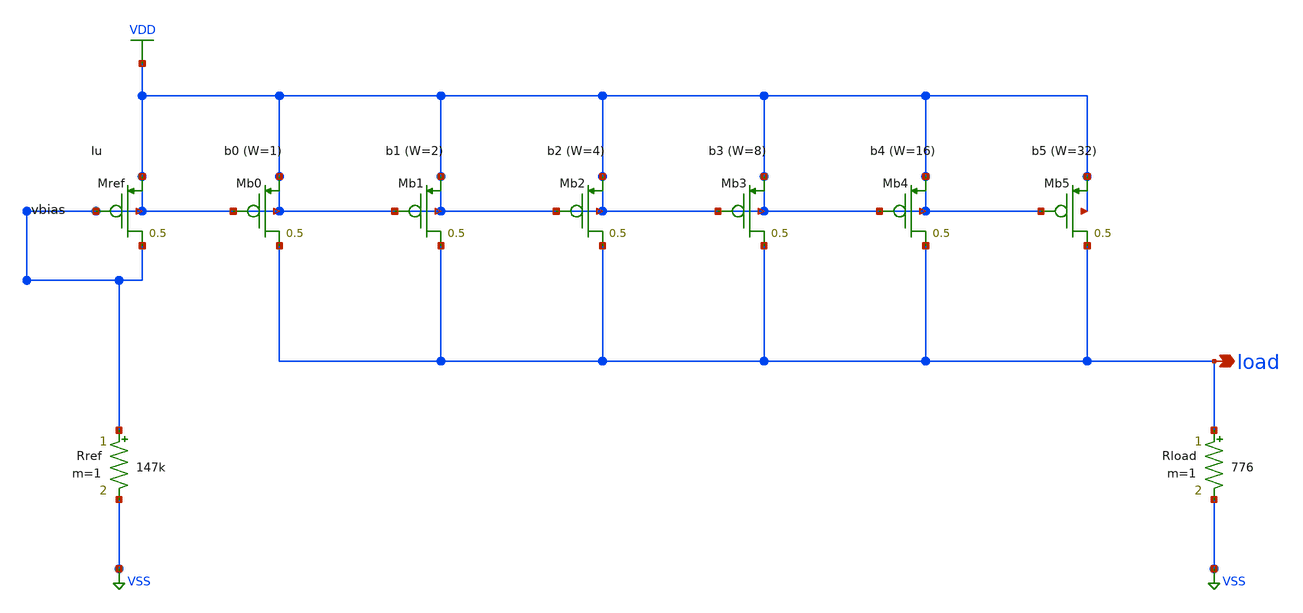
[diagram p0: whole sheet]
** sch_path: eda/hero/schematics/current_steering_dac.sch
**.subckt current_steering_dac load
*.opin load
XMref VDD VDD VDD VDD sky130_fd_pr__sky130_fd_pr__pfet_01v8 L=0.5 W=1 nrd='0.29 / W' nrs='0.29 / W' sa=0
+ sb=0 sd=0 mult=1 m=1
XMb0 load VDD VDD VDD sky130_fd_pr__sky130_fd_pr__pfet_01v8 L=0.5 W=1 nrd='0.29 / W' nrs='0.29 / W' sa=0
+ sb=0 sd=0 mult=1 m=1
XMb1 load VDD VDD VDD sky130_fd_pr__sky130_fd_pr__pfet_01v8 L=0.5 W=2 nrd='0.29 / W' nrs='0.29 / W' sa=0
+ sb=0 sd=0 mult=1 m=1
XMb2 load VDD VDD VDD sky130_fd_pr__sky130_fd_pr__pfet_01v8 L=0.5 W=4 nrd='0.29 / W' nrs='0.29 / W' sa=0
+ sb=0 sd=0 mult=1 m=1
XMb3 load VDD VDD VDD sky130_fd_pr__sky130_fd_pr__pfet_01v8 L=0.5 W=8 nrd='0.29 / W' nrs='0.29 / W' sa=0
+ sb=0 sd=0 mult=1 m=1
XMb4 load VDD VDD VDD sky130_fd_pr__sky130_fd_pr__pfet_01v8 L=0.5 W=16 nrd='0.29 / W' nrs='0.29 / W'
+ sa=0 sb=0 sd=0 mult=1 m=1
XMb5 load VDD VDD VDD sky130_fd_pr__sky130_fd_pr__pfet_01v8 L=0.5 W=32 nrd='0.29 / W' nrs='0.29 / W'
+ sa=0 sb=0 sd=0 mult=1 m=1
Rref VDD VSS 147k m=1
Rload load VSS 776 m=1
**.ends
.GLOBAL VDD
.GLOBAL VSS
.end
